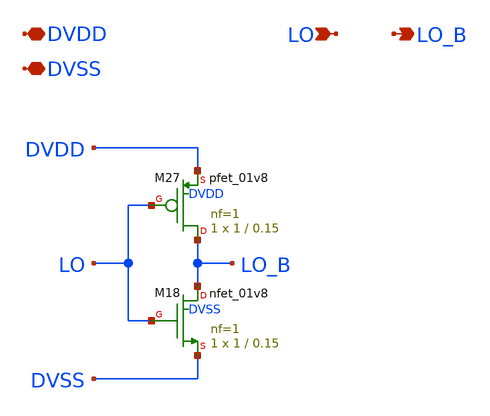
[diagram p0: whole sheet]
** sch_path: xschem/level_shifter_dd.sch
**.subckt level_shifter_dd DVDD DVSS LO LO_B
*.iopin DVDD
*.iopin DVSS
*.ipin LO
*.opin LO_B
XM18 LO_B LO DVSS DVSS sky130_fd_pr__nfet_01v8 L=0.15 W=1 nf=1 ad='int((nf+1)/2) * W/nf * 0.29' as='int((nf+2)/2) * W/nf * 0.29'
+ pd='2*int((nf+1)/2) * (W/nf + 0.29)' ps='2*int((nf+2)/2) * (W/nf + 0.29)' nrd='0.29 / W' nrs='0.29 / W'
+ sa=0 sb=0 sd=0 mult=1 m=1
XM27 LO_B LO DVDD DVDD sky130_fd_pr__pfet_01v8 L=0.15 W=1 nf=1 ad='int((1 + 1)/2) * 1 / 1 * 0.29' as='int((1 + 2)/2) * 1 / 1 * 0.29'
+ pd='2*int((1 + 1)/2) * (1 / 1 + 0.29)' ps='2*int((1 + 2)/2) * (1 / 1 + 0.29)' nrd='0.29 / 1 ' nrs='0.29 / 1 '
+ sa=0 sb=0 sd=0 mult=1 m=1
**.ends
.end
